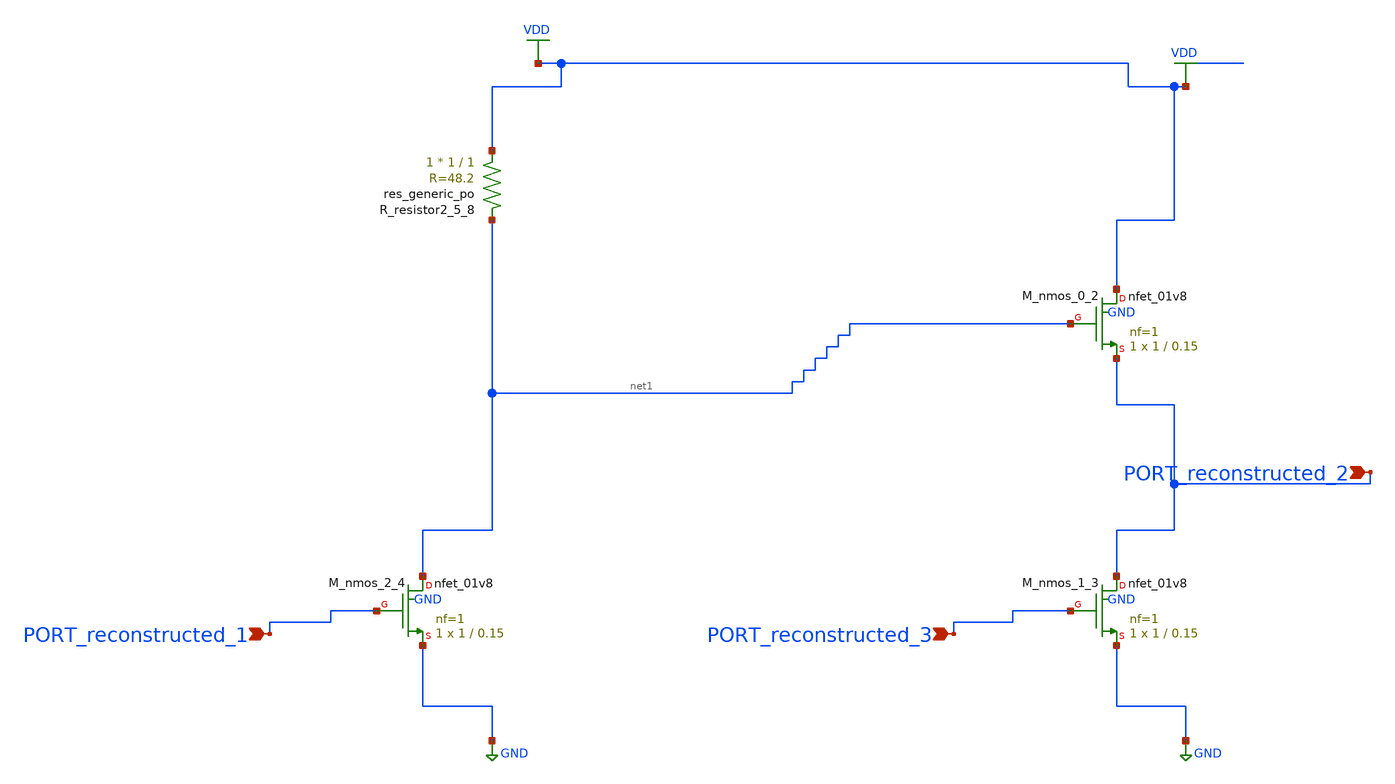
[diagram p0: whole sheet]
** sch_path: schematics/AMSNet/317.sch
**.subckt 317 PORT_reconstructed_2 PORT_reconstructed_3 PORT_reconstructed_1
*.ipin PORT_reconstructed_2
*.ipin PORT_reconstructed_3
*.ipin PORT_reconstructed_1
XM_nmos_0_2 VDD net1 PORT_reconstructed_2 GND sky130_fd_pr__nfet_01v8 L=0.15 W=1 nf=1 ad='int((1 + 1)/2) * 1 / 1 * 0.29'
+ as='int((1 + 2)/2) * 1 / 1 * 0.29' pd='2*int((1 + 1)/2) * (1 / 1 + 0.29)' ps='2*int((1 + 2)/2) * (1 / 1 + 0.29)'
+ nrd='0.29 / 1 ' nrs='0.29 / 1 ' sa=0 sb=0 sd=0 mult=1 m=1
XM_nmos_1_3 PORT_reconstructed_2 PORT_reconstructed_3 GND GND sky130_fd_pr__nfet_01v8 L=0.15 W=1 nf=1
+ ad='int((1 + 1)/2) * 1 / 1 * 0.29' as='int((1 + 2)/2) * 1 / 1 * 0.29' pd='2*int((1 + 1)/2) * (1 / 1 + 0.29)'
+ ps='2*int((1 + 2)/2) * (1 / 1 + 0.29)' nrd='0.29 / 1 ' nrs='0.29 / 1 ' sa=0 sb=0 sd=0 mult=1 m=1
XM_nmos_2_4 net1 PORT_reconstructed_1 GND GND sky130_fd_pr__nfet_01v8 L=0.15 W=1 nf=1 ad='int((1 + 1)/2) * 1 / 1 * 0.29'
+ as='int((1 + 2)/2) * 1 / 1 * 0.29' pd='2*int((1 + 1)/2) * (1 / 1 + 0.29)' ps='2*int((1 + 2)/2) * (1 / 1 + 0.29)'
+ nrd='0.29 / 1 ' nrs='0.29 / 1 ' sa=0 sb=0 sd=0 mult=1 m=1
XR_resistor2_5_8 VDD net1 sky130_fd_pr__res_generic_po W=1 L=1 m=1
**.ends
.GLOBAL GND
.GLOBAL VDD
.end
